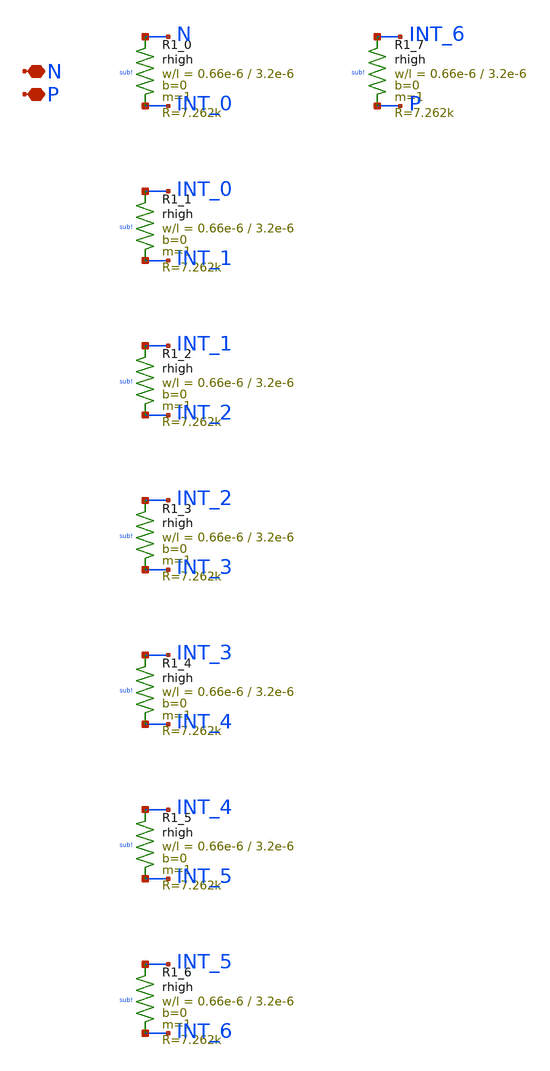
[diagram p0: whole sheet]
** sch_path: design/LELO_TR_IHP13G2/LELOTR_RES8.sch
**.subckt LELOTR_RES8 N P
*.iopin N
*.iopin P
XR1_0 N INT_0 sub! rhigh w=0.66e-6 l=3.2e-6 m=1 b=0 mm_ok=1
XR1_1 INT_0 INT_1 sub! rhigh w=0.66e-6 l=3.2e-6 m=1 b=0 mm_ok=1
XR1_2 INT_1 INT_2 sub! rhigh w=0.66e-6 l=3.2e-6 m=1 b=0 mm_ok=1
XR1_3 INT_2 INT_3 sub! rhigh w=0.66e-6 l=3.2e-6 m=1 b=0 mm_ok=1
XR1_4 INT_3 INT_4 sub! rhigh w=0.66e-6 l=3.2e-6 m=1 b=0 mm_ok=1
XR1_5 INT_4 INT_5 sub! rhigh w=0.66e-6 l=3.2e-6 m=1 b=0 mm_ok=1
XR1_6 INT_5 INT_6 sub! rhigh w=0.66e-6 l=3.2e-6 m=1 b=0 mm_ok=1
XR1_7 INT_6 P sub! rhigh w=0.66e-6 l=3.2e-6 m=1 b=0 mm_ok=1
**.ends
.end
